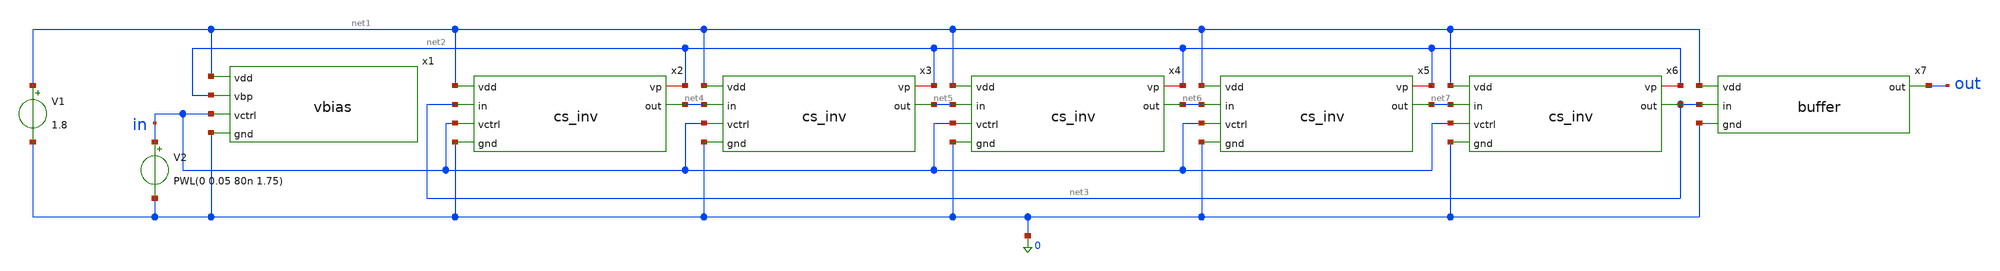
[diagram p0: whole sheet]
** sch_path: vcro/vcro_final.sch
**.subckt vcro_final
V1 net1 0 1.8
V2 in 0 PWL(0 0.05 80n 1.75)
x1 net1 net2 in 0 vbias
x2 net1 net2 net3 net4 in 0 cs_inv
x3 net1 net2 net4 net5 in 0 cs_inv
x4 net1 net2 net5 net6 in 0 cs_inv
x5 net1 net2 net6 net7 in 0 cs_inv
x6 net1 net2 net7 net3 in 0 cs_inv
x7 net1 net3 out 0 buffer
**** begin user architecture code
 .lib /foss/pdks/sky130A/libs.tech/ngspice/sky130.lib.spice tt

.param mc_mm_switch=0
.param mc_pr_switch=1



.option wnflag=0
.option savecurrents

.control
save all
tran 0.01n 80n
plot v(out) v(in)
.endc


**** end user architecture code
**.ends
.end
